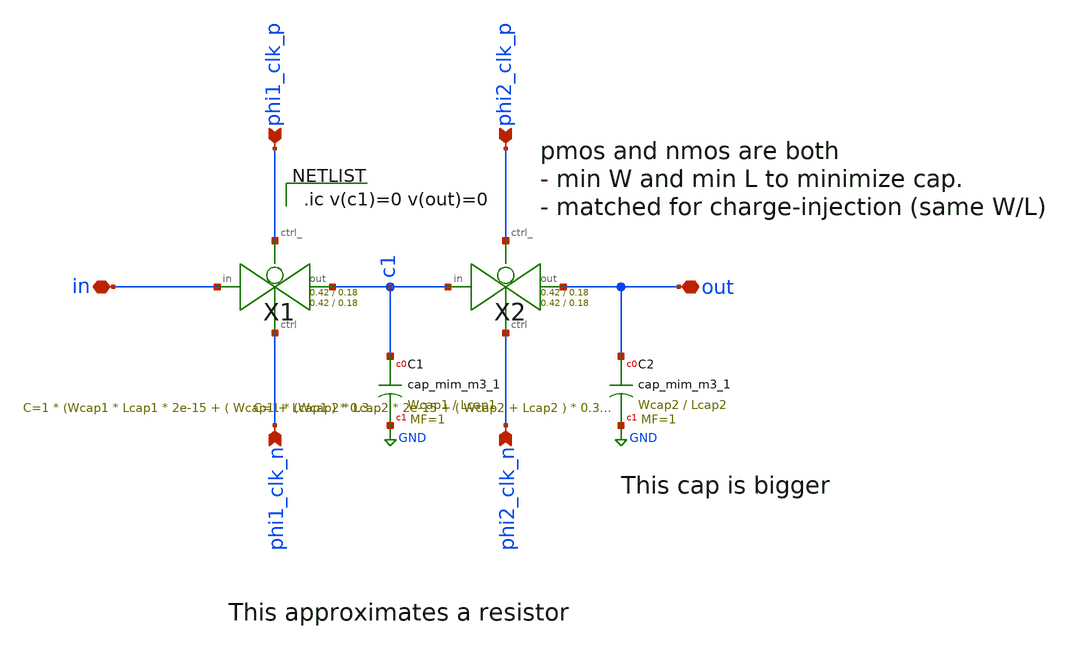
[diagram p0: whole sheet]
** sch_path: xschem/Switched_Caps/2switchcaps.sch
**.subckt 2switchcaps out in phi1_clk_n phi1_clk_p phi2_clk_p phi2_clk_n
*.iopin out
*.iopin in
*.ipin phi1_clk_n
*.ipin phi1_clk_p
*.ipin phi2_clk_p
*.ipin phi2_clk_n
XC1 c1 GND sky130_fd_pr__cap_mim_m3_1 W=Wcap1 L=Lcap1 MF=1 m=1
XC2 out GND sky130_fd_pr__cap_mim_m3_1 W=Wcap2 L=Lcap2 MF=1 m=1
X1 in c1 phi1_clk_p phi1_clk_n transmission_gate Wpmos=0.42 Lpmos=0.18 Wnmos=0.42 Lnmos=0.18
X2 c1 out phi2_clk_p phi2_clk_n transmission_gate Wpmos=0.42 Lpmos=0.18 Wnmos=0.42 Lnmos=0.18
**** begin user architecture code

.ic v(c1)=0 v(out)=0

**** end user architecture code
**.ends

* expanding   symbol:  transmission_gate/transmission_gate.sym # of pins=4
** sym_path: xschem/transmission_gate/transmission_gate.sym
** sch_path: xschem/transmission_gate/transmission_gate.sch
.subckt transmission_gate in out ctrl_ ctrl  Wpmos=0.42 Lpmos=0.18 Wnmos=0.42 Lnmos=0.18
*.iopin in
*.iopin out
*.ipin ctrl_
*.ipin ctrl
XM1 out ctrl in GND sky130_fd_pr__nfet_01v8 L=Lnmos W=Wnmos nf=1 ad='int((nf+1)/2) * W/nf * 0.29' as='int((nf+2)/2) * W/nf * 0.29'
+ pd='2*int((nf+1)/2) * (W/nf + 0.29)' ps='2*int((nf+2)/2) * (W/nf + 0.29)' nrd='0.29 / W' nrs='0.29 / W'
+ sa=0 sb=0 sd=0 mult=1 m=1
XM2 out ctrl_ in VDD sky130_fd_pr__pfet_01v8 L=Lpmos W=Wpmos nf=1 ad='int((nf+1)/2) * W/nf * 0.29' as='int((nf+2)/2) * W/nf * 0.29'
+ pd='2*int((nf+1)/2) * (W/nf + 0.29)' ps='2*int((nf+2)/2) * (W/nf + 0.29)' nrd='0.29 / W' nrs='0.29 / W'
+ sa=0 sb=0 sd=0 mult=1 m=1
.ends

.GLOBAL GND
.GLOBAL VDD
.end
